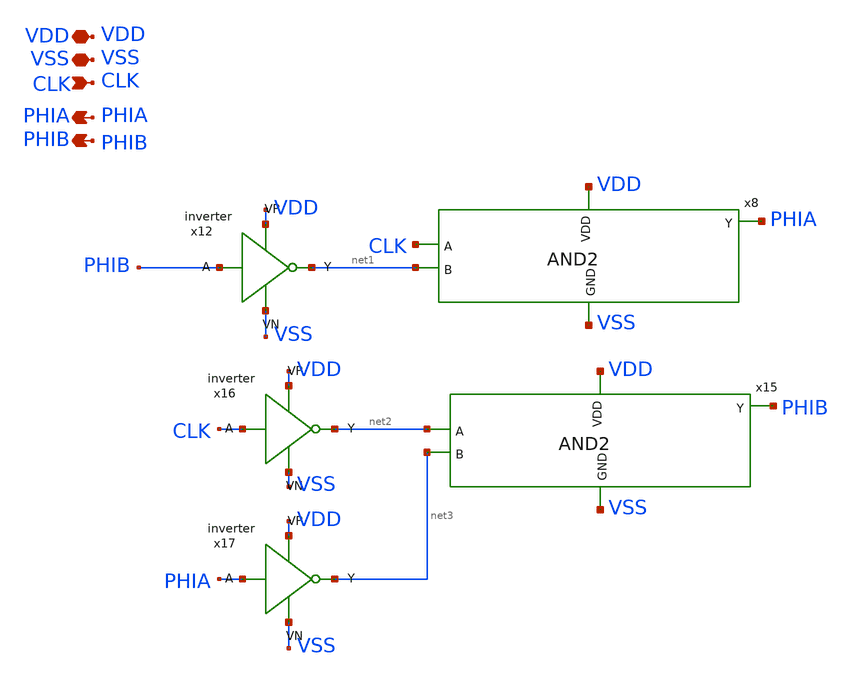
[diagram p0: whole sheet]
** sch_path: ADC/4bit_C2C/MagicAndSpice/SARclkgen.sch
**.subckt SARclkgen VSS CLK PHIA PHIB VDD
*.iopin VSS
*.ipin CLK
*.opin PHIA
*.opin PHIB
*.iopin VDD
x8 VDD PHIA CLK net1 VSS AND2
x12 PHIB net1 VDD VSS inverter
x15 VDD PHIB net2 net3 VSS AND2
x16 CLK net2 VDD VSS inverter
x17 PHIA net3 VDD VSS inverter
**.ends
.end
